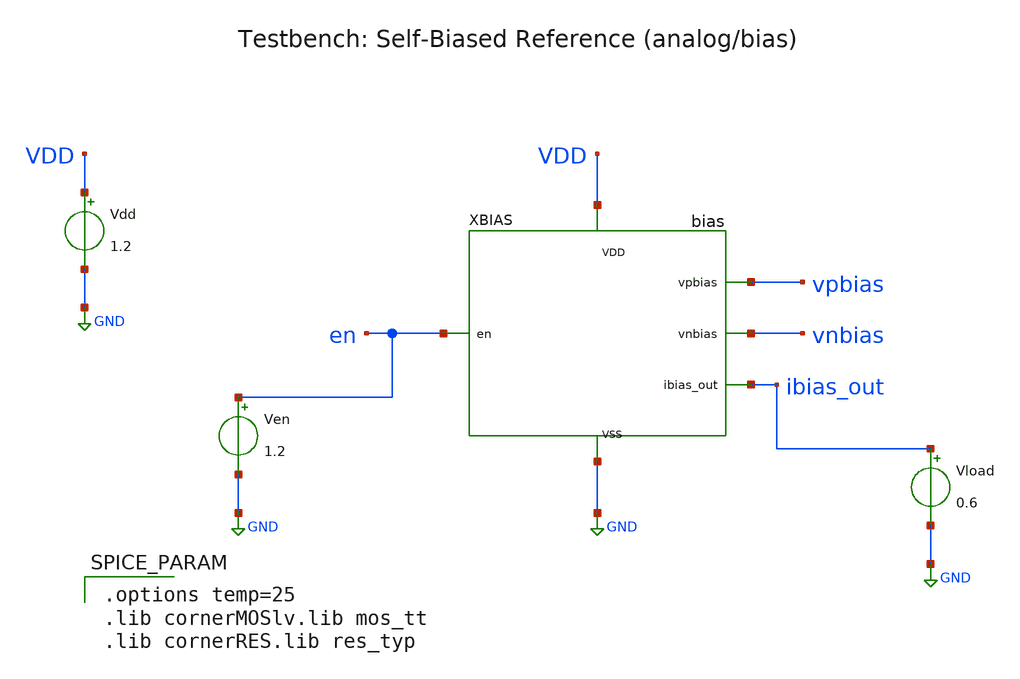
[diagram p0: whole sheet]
** sch_path: analog/bias/tb_bias.sch
**.subckt tb_bias
XBIAS VDD GND en vpbias vnbias ibias_out bias
Vdd VDD GND 1.2
Ven en GND 1.2
Vload ibias_out GND 0.6
**** begin user architecture code

.options temp=25
.lib cornerMOSlv.lib mos_tt
.lib cornerRES.lib res_typ


**** end user architecture code
**.ends

* expanding   symbol:  bias/bias.sym # of pins=6
** sym_path: analog/bias/bias.sym
** sch_path: analog/bias/bias.sch
.subckt bias VDD VSS en vpbias vnbias ibias_out
*.iopin VDD
*.iopin VSS
*.ipin en
*.opin vpbias
*.opin vnbias
*.opin ibias_out
XMEN_P enb en VDD VDD sg13_lv_pmos w=0.5u l=0.5u ng=1 m=1 mm_ok=1
XMEN_N enb en VSS VSS sg13_lv_nmos w=0.25u l=0.5u ng=1 m=1 mm_ok=1
XMSU_EN net1 enb VDD VDD sg13_lv_pmos w=0.3u l=1.0u ng=1 m=1 mm_ok=1
XMSU_P1 net2 VSS net1 VDD sg13_lv_pmos w=0.15u l=10u ng=1 m=1 mm_ok=1
XMSU_P2 net3 VSS net2 VDD sg13_lv_pmos w=0.15u l=10u ng=1 m=1 mm_ok=1
XMSU_N net3 vnbias VSS VSS sg13_lv_nmos w=4.0u l=0.5u ng=1 m=1 mm_ok=1
XMSU_INJ vpbias net3 VSS VSS sg13_lv_nmos w=0.5u l=1.0u ng=1 m=1 mm_ok=1
XMP1 vnbias vpbias VDD VDD sg13_lv_pmos w=1.0u l=4.0u ng=1 m=1 mm_ok=1
XMN1 vnbias vnbias VSS VSS sg13_lv_nmos w=0.3u l=4.0u ng=1 m=1 mm_ok=1
XMP2 vpbias vpbias VDD VDD sg13_lv_pmos w=1.0u l=4.0u ng=1 m=1 mm_ok=1
XMN2 vpbias vnbias net4 VSS sg13_lv_nmos w=0.3u l=4.0u ng=1 m=4 mm_ok=1
XR_BIAS net4 VSS VSS rppd w=0.5e-6 l=20.0e-6 m=1 b=19 mm_ok=1
XMP_OFF vpbias en VDD VDD sg13_lv_pmos w=1.0u l=0.5u ng=1 m=1 mm_ok=1
XMN_OFF vnbias enb VSS VSS sg13_lv_nmos w=1.0u l=0.5u ng=1 m=1 mm_ok=1
XMP_OUT ibias_out vpbias VDD VDD sg13_lv_pmos w=1.0u l=4.0u ng=1 m=1 mm_ok=1
.ends

.GLOBAL GND
.end
